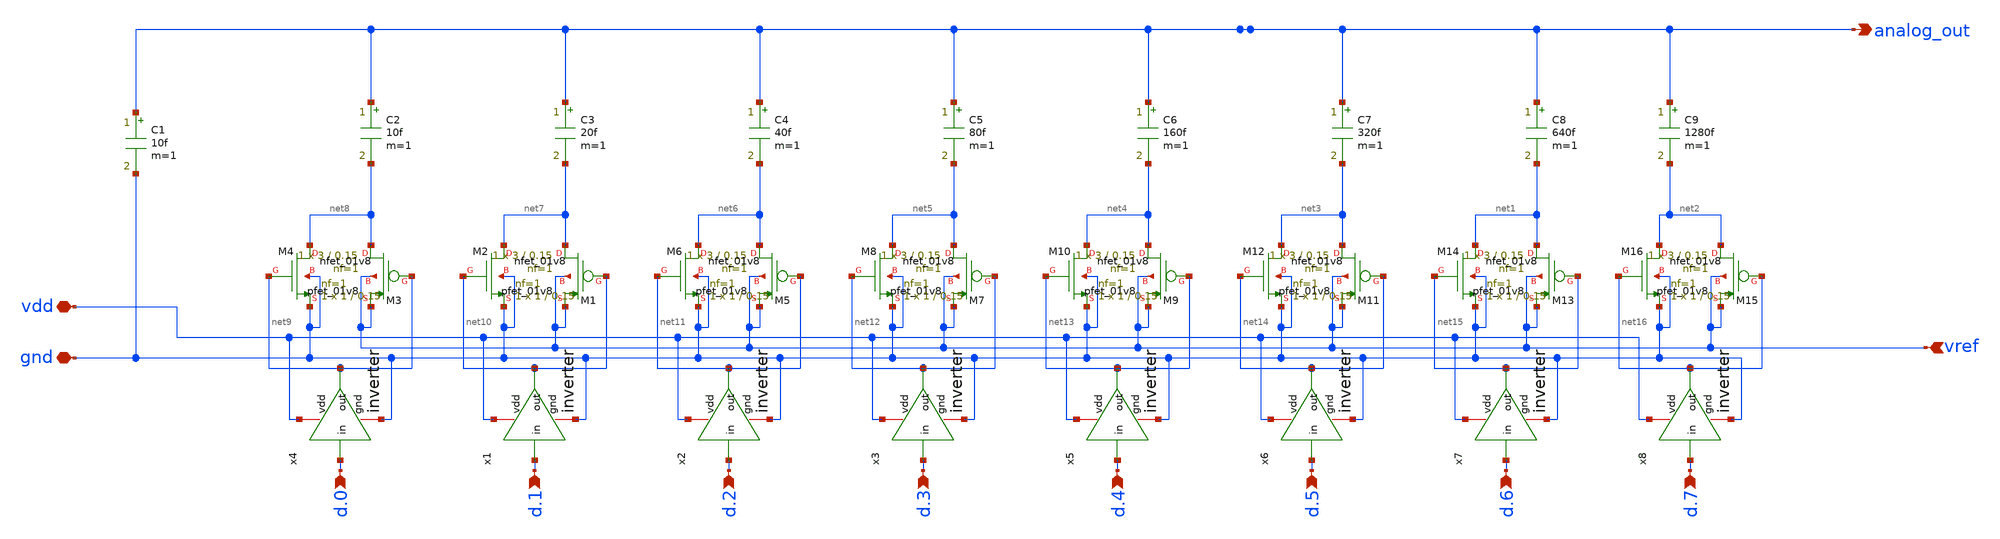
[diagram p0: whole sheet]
** sch_path: ideal_dac.sch
**.subckt ideal_dac d.0 d.1 d.2 d.3 d.4 d.5 d.6 d.7 vref analog_out gnd vdd
*.ipin d.0
*.ipin d.1
*.ipin d.2
*.ipin d.3
*.ipin d.4
*.ipin d.5
*.ipin d.6
*.ipin d.7
*.ipin vref
*.opin analog_out
*.iopin gnd
*.iopin vdd
x4 vdd d.0 net9 gnd inverter
XM3 net8 net9 vref vref sky130_fd_pr__pfet_01v8 L=0.15 W=3 nf=1 ad='int((nf+1)/2) * W/nf * 0.29' as='int((nf+2)/2) * W/nf * 0.29'
+ pd='2*int((nf+1)/2) * (W/nf + 0.29)' ps='2*int((nf+2)/2) * (W/nf + 0.29)' nrd='0.29 / W' nrs='0.29 / W'
+ sa=0 sb=0 sd=0 mult=1 m=1
XM4 net8 net9 gnd gnd sky130_fd_pr__nfet_01v8 L=0.15 W=1 nf=1 ad='int((1 + 1)/2) * 1 / 1 * 0.29' as='int((1 + 2)/2) * 1 / 1 * 0.29'
+ pd='2*int((1 + 1)/2) * (1 / 1 + 0.29)' ps='2*int((1 + 2)/2) * (1 / 1 + 0.29)' nrd='0.29 / 1 ' nrs='0.29 / 1 '
+ sa=0 sb=0 sd=0 mult=1 m=1
x1 vdd d.1 net10 gnd inverter
XM1 net7 net10 vref vref sky130_fd_pr__pfet_01v8 L=0.15 W=3 nf=1 ad='int((nf+1)/2) * W/nf * 0.29' as='int((nf+2)/2) * W/nf * 0.29'
+ pd='2*int((nf+1)/2) * (W/nf + 0.29)' ps='2*int((nf+2)/2) * (W/nf + 0.29)' nrd='0.29 / W' nrs='0.29 / W'
+ sa=0 sb=0 sd=0 mult=1 m=1
XM2 net7 net10 gnd gnd sky130_fd_pr__nfet_01v8 L=0.15 W=1 nf=1 ad='int((1 + 1)/2) * 1 / 1 * 0.29' as='int((1 + 2)/2) * 1 / 1 * 0.29'
+ pd='2*int((1 + 1)/2) * (1 / 1 + 0.29)' ps='2*int((1 + 2)/2) * (1 / 1 + 0.29)' nrd='0.29 / 1 ' nrs='0.29 / 1 '
+ sa=0 sb=0 sd=0 mult=1 m=1
x2 vdd d.2 net11 gnd inverter
XM5 net6 net11 vref vref sky130_fd_pr__pfet_01v8 L=0.15 W=3 nf=1 ad='int((nf+1)/2) * W/nf * 0.29' as='int((nf+2)/2) * W/nf * 0.29'
+ pd='2*int((nf+1)/2) * (W/nf + 0.29)' ps='2*int((nf+2)/2) * (W/nf + 0.29)' nrd='0.29 / W' nrs='0.29 / W'
+ sa=0 sb=0 sd=0 mult=1 m=1
XM6 net6 net11 gnd gnd sky130_fd_pr__nfet_01v8 L=0.15 W=1 nf=1 ad='int((1 + 1)/2) * 1 / 1 * 0.29' as='int((1 + 2)/2) * 1 / 1 * 0.29'
+ pd='2*int((1 + 1)/2) * (1 / 1 + 0.29)' ps='2*int((1 + 2)/2) * (1 / 1 + 0.29)' nrd='0.29 / 1 ' nrs='0.29 / 1 '
+ sa=0 sb=0 sd=0 mult=1 m=1
x3 vdd d.3 net12 gnd inverter
XM7 net5 net12 vref vref sky130_fd_pr__pfet_01v8 L=0.15 W=3 nf=1 ad='int((nf+1)/2) * W/nf * 0.29' as='int((nf+2)/2) * W/nf * 0.29'
+ pd='2*int((nf+1)/2) * (W/nf + 0.29)' ps='2*int((nf+2)/2) * (W/nf + 0.29)' nrd='0.29 / W' nrs='0.29 / W'
+ sa=0 sb=0 sd=0 mult=1 m=1
XM8 net5 net12 gnd gnd sky130_fd_pr__nfet_01v8 L=0.15 W=1 nf=1 ad='int((1 + 1)/2) * 1 / 1 * 0.29' as='int((1 + 2)/2) * 1 / 1 * 0.29'
+ pd='2*int((1 + 1)/2) * (1 / 1 + 0.29)' ps='2*int((1 + 2)/2) * (1 / 1 + 0.29)' nrd='0.29 / 1 ' nrs='0.29 / 1 '
+ sa=0 sb=0 sd=0 mult=1 m=1
x5 vdd d.4 net13 gnd inverter
XM9 net4 net13 vref vref sky130_fd_pr__pfet_01v8 L=0.15 W=3 nf=1 ad='int((nf+1)/2) * W/nf * 0.29' as='int((nf+2)/2) * W/nf * 0.29'
+ pd='2*int((nf+1)/2) * (W/nf + 0.29)' ps='2*int((nf+2)/2) * (W/nf + 0.29)' nrd='0.29 / W' nrs='0.29 / W'
+ sa=0 sb=0 sd=0 mult=1 m=1
XM10 net4 net13 gnd gnd sky130_fd_pr__nfet_01v8 L=0.15 W=1 nf=1 ad='int((1 + 1)/2) * 1 / 1 * 0.29' as='int((1 + 2)/2) * 1 / 1 * 0.29'
+ pd='2*int((1 + 1)/2) * (1 / 1 + 0.29)' ps='2*int((1 + 2)/2) * (1 / 1 + 0.29)' nrd='0.29 / 1 ' nrs='0.29 / 1 '
+ sa=0 sb=0 sd=0 mult=1 m=1
x6 vdd d.5 net14 gnd inverter
XM11 net3 net14 vref vref sky130_fd_pr__pfet_01v8 L=0.15 W=3 nf=1 ad='int((nf+1)/2) * W/nf * 0.29' as='int((nf+2)/2) * W/nf * 0.29'
+ pd='2*int((nf+1)/2) * (W/nf + 0.29)' ps='2*int((nf+2)/2) * (W/nf + 0.29)' nrd='0.29 / W' nrs='0.29 / W'
+ sa=0 sb=0 sd=0 mult=1 m=1
XM12 net3 net14 gnd gnd sky130_fd_pr__nfet_01v8 L=0.15 W=1 nf=1 ad='int((1 + 1)/2) * 1 / 1 * 0.29' as='int((1 + 2)/2) * 1 / 1 * 0.29'
+ pd='2*int((1 + 1)/2) * (1 / 1 + 0.29)' ps='2*int((1 + 2)/2) * (1 / 1 + 0.29)' nrd='0.29 / 1 ' nrs='0.29 / 1 '
+ sa=0 sb=0 sd=0 mult=1 m=1
x7 vdd d.6 net15 gnd inverter
XM13 net1 net15 vref vref sky130_fd_pr__pfet_01v8 L=0.15 W=3 nf=1 ad='int((nf+1)/2) * W/nf * 0.29' as='int((nf+2)/2) * W/nf * 0.29'
+ pd='2*int((nf+1)/2) * (W/nf + 0.29)' ps='2*int((nf+2)/2) * (W/nf + 0.29)' nrd='0.29 / W' nrs='0.29 / W'
+ sa=0 sb=0 sd=0 mult=1 m=1
XM14 net1 net15 gnd gnd sky130_fd_pr__nfet_01v8 L=0.15 W=1 nf=1 ad='int((1 + 1)/2) * 1 / 1 * 0.29' as='int((1 + 2)/2) * 1 / 1 * 0.29'
+ pd='2*int((1 + 1)/2) * (1 / 1 + 0.29)' ps='2*int((1 + 2)/2) * (1 / 1 + 0.29)' nrd='0.29 / 1 ' nrs='0.29 / 1 '
+ sa=0 sb=0 sd=0 mult=1 m=1
x8 vdd d.7 net16 gnd inverter
XM15 net2 net16 vref vref sky130_fd_pr__pfet_01v8 L=0.15 W=3 nf=1 ad='int((nf+1)/2) * W/nf * 0.29' as='int((nf+2)/2) * W/nf * 0.29'
+ pd='2*int((nf+1)/2) * (W/nf + 0.29)' ps='2*int((nf+2)/2) * (W/nf + 0.29)' nrd='0.29 / W' nrs='0.29 / W'
+ sa=0 sb=0 sd=0 mult=1 m=1
XM16 net2 net16 gnd gnd sky130_fd_pr__nfet_01v8 L=0.15 W=1 nf=1 ad='int((1 + 1)/2) * 1 / 1 * 0.29' as='int((1 + 2)/2) * 1 / 1 * 0.29'
+ pd='2*int((1 + 1)/2) * (1 / 1 + 0.29)' ps='2*int((1 + 2)/2) * (1 / 1 + 0.29)' nrd='0.29 / 1 ' nrs='0.29 / 1 '
+ sa=0 sb=0 sd=0 mult=1 m=1
C1 analog_out gnd 10f m=1
C2 analog_out net8 10f m=1
C3 analog_out net7 20f m=1
C4 analog_out net6 40f m=1
C5 analog_out net5 80f m=1
C6 analog_out net4 160f m=1
C7 analog_out net3 320f m=1
C8 analog_out net1 640f m=1
C9 analog_out net2 1280f m=1
**.ends

* expanding   symbol:  /foss/designs/sar_adc/inverter.sym # of pins=4
** sym_path: inverter.sym
** sch_path: inverter.sch
.subckt inverter vdd in out gnd
*.iopin vdd
*.iopin gnd
*.ipin in
*.opin out
XM2 out in gnd gnd sky130_fd_pr__nfet_01v8 L=0.15 W=1 nf=1 ad='int((1 + 1)/2) * 1 / 1 * 0.29' as='int((1 + 2)/2) * 1 / 1 * 0.29'
+ pd='2*int((1 + 1)/2) * (1 / 1 + 0.29)' ps='2*int((1 + 2)/2) * (1 / 1 + 0.29)' nrd='0.29 / 1 ' nrs='0.29 / 1 '
+ sa=0 sb=0 sd=0 mult=1 m=1
XM11 out in vdd vdd sky130_fd_pr__pfet_01v8 L=0.15 W=3 nf=1 ad='int((nf+1)/2) * W/nf * 0.29' as='int((nf+2)/2) * W/nf * 0.29'
+ pd='2*int((nf+1)/2) * (W/nf + 0.29)' ps='2*int((nf+2)/2) * (W/nf + 0.29)' nrd='0.29 / W' nrs='0.29 / W'
+ sa=0 sb=0 sd=0 mult=1 m=1
.ends

.end
